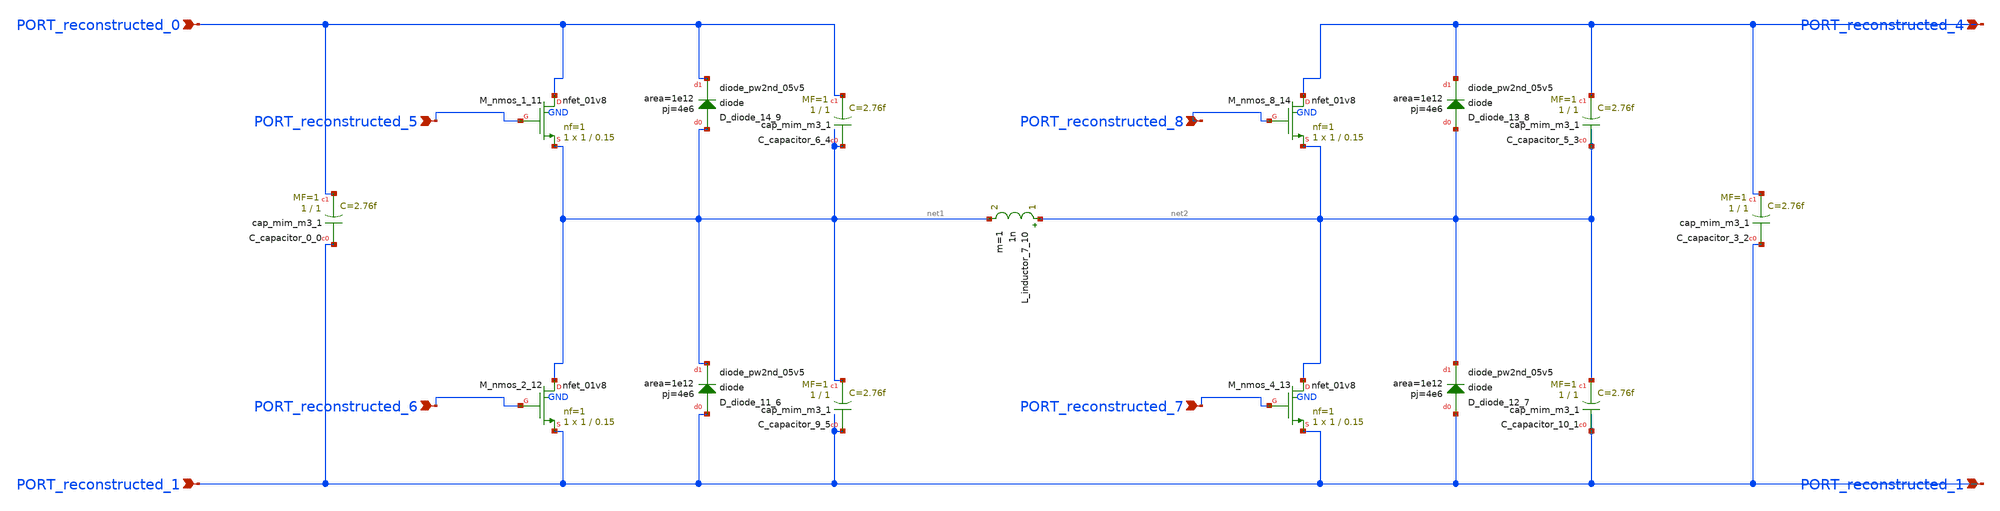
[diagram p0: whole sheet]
** sch_path: schematics/10_1109_ACCESS_2019_2903841_01_001_canvas.sch
**.subckt 10_1109_ACCESS_2019_2903841_01_001_canvas PORT_reconstructed_0 PORT_reconstructed_1
*+ PORT_reconstructed_4 PORT_reconstructed_1 PORT_reconstructed_6 PORT_reconstructed_7 PORT_reconstructed_5
*+ PORT_reconstructed_8
*.ipin PORT_reconstructed_0
*.ipin PORT_reconstructed_1
*.ipin PORT_reconstructed_4
*.ipin PORT_reconstructed_1
*.ipin PORT_reconstructed_6
*.ipin PORT_reconstructed_7
*.ipin PORT_reconstructed_5
*.ipin PORT_reconstructed_8
XC_capacitor_0_0 PORT_reconstructed_1 PORT_reconstructed_0 sky130_fd_pr__cap_mim_m3_1 W=1 L=1 MF=1
+ m=1
XC_capacitor_10_1 PORT_reconstructed_1 net2 sky130_fd_pr__cap_mim_m3_1 W=1 L=1 MF=1 m=1
XC_capacitor_3_2 PORT_reconstructed_1 PORT_reconstructed_4 sky130_fd_pr__cap_mim_m3_1 W=1 L=1 MF=1
+ m=1
XC_capacitor_5_3 net2 PORT_reconstructed_4 sky130_fd_pr__cap_mim_m3_1 W=1 L=1 MF=1 m=1
XC_capacitor_6_4 net1 PORT_reconstructed_0 sky130_fd_pr__cap_mim_m3_1 W=1 L=1 MF=1 m=1
XC_capacitor_9_5 PORT_reconstructed_1 net1 sky130_fd_pr__cap_mim_m3_1 W=1 L=1 MF=1 m=1
XD_diode_11_6 PORT_reconstructed_1 net1 sky130_fd_pr__diode_pw2nd_05v5 area=1e12 pj=4e6
XD_diode_12_7 PORT_reconstructed_1 net2 sky130_fd_pr__diode_pw2nd_05v5 area=1e12 pj=4e6
XD_diode_13_8 net2 PORT_reconstructed_4 sky130_fd_pr__diode_pw2nd_05v5 area=1e12 pj=4e6
XD_diode_14_9 net1 PORT_reconstructed_0 sky130_fd_pr__diode_pw2nd_05v5 area=1e12 pj=4e6
L_inductor_7_10 net2 net1 1n m=1
XM_nmos_1_11 PORT_reconstructed_0 PORT_reconstructed_5 net1 GND sky130_fd_pr__nfet_01v8 L=0.15 W=1 nf=1
+ ad='int((1 + 1)/2) * 1 / 1 * 0.29' as='int((1 + 2)/2) * 1 / 1 * 0.29' pd='2*int((1 + 1)/2) * (1 / 1 + 0.29)'
+ ps='2*int((1 + 2)/2) * (1 / 1 + 0.29)' nrd='0.29 / 1 ' nrs='0.29 / 1 ' sa=0 sb=0 sd=0 mult=1 m=1
XM_nmos_2_12 net1 PORT_reconstructed_6 PORT_reconstructed_1 GND sky130_fd_pr__nfet_01v8 L=0.15 W=1 nf=1
+ ad='int((1 + 1)/2) * 1 / 1 * 0.29' as='int((1 + 2)/2) * 1 / 1 * 0.29' pd='2*int((1 + 1)/2) * (1 / 1 + 0.29)'
+ ps='2*int((1 + 2)/2) * (1 / 1 + 0.29)' nrd='0.29 / 1 ' nrs='0.29 / 1 ' sa=0 sb=0 sd=0 mult=1 m=1
XM_nmos_4_13 net2 PORT_reconstructed_7 PORT_reconstructed_1 GND sky130_fd_pr__nfet_01v8 L=0.15 W=1 nf=1
+ ad='int((1 + 1)/2) * 1 / 1 * 0.29' as='int((1 + 2)/2) * 1 / 1 * 0.29' pd='2*int((1 + 1)/2) * (1 / 1 + 0.29)'
+ ps='2*int((1 + 2)/2) * (1 / 1 + 0.29)' nrd='0.29 / 1 ' nrs='0.29 / 1 ' sa=0 sb=0 sd=0 mult=1 m=1
XM_nmos_8_14 PORT_reconstructed_4 PORT_reconstructed_8 net2 GND sky130_fd_pr__nfet_01v8 L=0.15 W=1 nf=1
+ ad='int((1 + 1)/2) * 1 / 1 * 0.29' as='int((1 + 2)/2) * 1 / 1 * 0.29' pd='2*int((1 + 1)/2) * (1 / 1 + 0.29)'
+ ps='2*int((1 + 2)/2) * (1 / 1 + 0.29)' nrd='0.29 / 1 ' nrs='0.29 / 1 ' sa=0 sb=0 sd=0 mult=1 m=1
**.ends
.end
